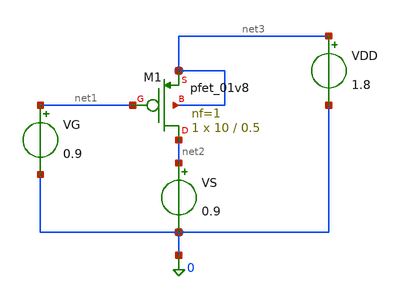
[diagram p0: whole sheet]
** sch_path: schematics/pmos.sch
**.subckt pmos
VG net1 0 0.9
VDD net3 0 1.8
VS net2 0 0.9
XM1 net2 net1 net3 net3 sky130_fd_pr__pfet_01v8 L=0.5 W=10 nf=1 ad='int((1 + 1)/2) * 10 / 1 * 0.29' as='int((1 + 2)/2) * 10 / 1 * 0.29'
+ pd='2*int((1 + 1)/2) * (10 / 1 + 0.29)' ps='2*int((1 + 2)/2) * (10 / 1 + 0.29)' nrd='0.29 / 10 ' nrs='0.29 / 10 '
+ sa=0 sb=0 sd=0 mult=1 m=1
**** begin user architecture code

.lib /usr/local/share/pdk/sky130A/libs.tech/ngspice/sky130.lib.spice tt

.control
  * 1. Save internal parameters BEFORE the sweep
  save @m.xm1.msky130_fd_pr__pfet_01v8[id]
  save @m.xm1.msky130_fd_pr__pfet_01v8[gm]
  save @m.xm1.msky130_fd_pr__pfet_01v8[gds]
  save @m.xm1.msky130_fd_pr__pfet_01v8[cgg]
  save all

  * 2. Sweep VG from 1.8V down to 0V (Negative Step)
  dc VG 1.8 0 -0.01

  * 3. Assign vectors (using abs() for ID)
  let id_vec = abs(@m.xm1.msky130_fd_pr__pfet_01v8[id])
  let gm_vec = @m.xm1.msky130_fd_pr__pfet_01v8[gm]
  let gds_vec = @m.xm1.msky130_fd_pr__pfet_01v8[gds]
  let cgg_vec = @m.xm1.msky130_fd_pr__pfet_01v8[cgg]

  * 4. Calculate the metrics
  let gm_id = gm_vec / id_vec
  let id_w = id_vec / 10u
  let intrinsic_gain = gm_vec / gds_vec
  let fT = gm_vec / (2 * 3.14159 * cgg_vec)

  * 5. Plot the graphs
  plot id_w vs gm_id
  plot intrinsic_gain vs gm_id
  plot fT vs gm_id
.endc

**** end user architecture code
**.ends
.end
